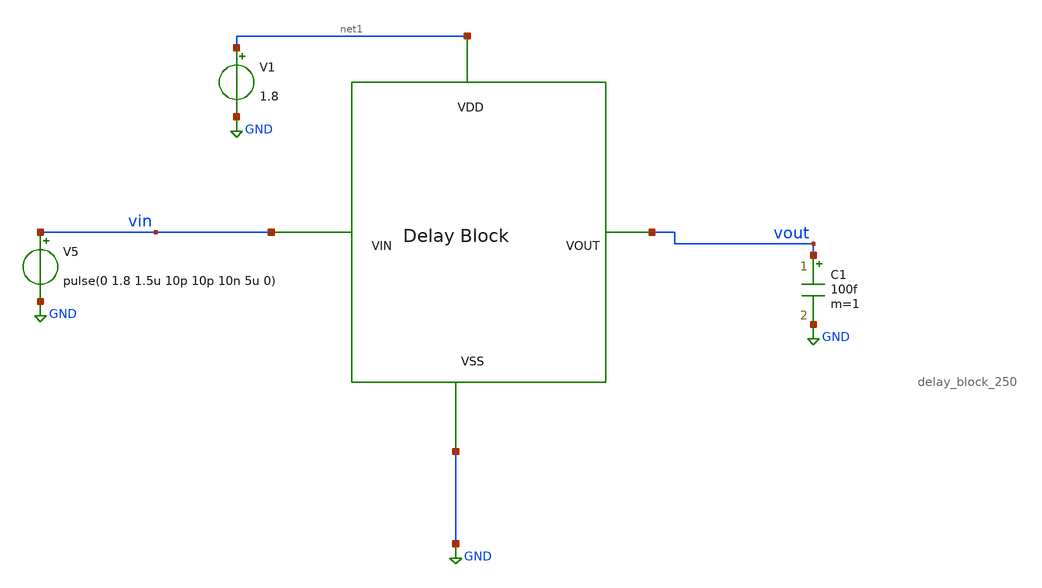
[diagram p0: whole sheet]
** sch_path: xschem/DC_DC_Converter_xschem/DC_DC_Converter/Delay_block_revised/previous/delay_bpock_tb.sch
**.subckt delay_bpock_tb
V1 net1 GND 1.8
V5 vin GND pulse(0 1.8 1.5u 10p 10p 10n 5u 0)
C1 vout GND 100f m=1
x1 net1 vin vout GND delay_block_250
**** begin user architecture code


.control
tran 0.01u 5u
plot v(vin) v(vout)

.endc



** opencircuitdesign pdks install
.lib $::SKYWATER_MODELS/sky130.lib.spice tt


**** end user architecture code
**.ends
.GLOBAL GND
.end
